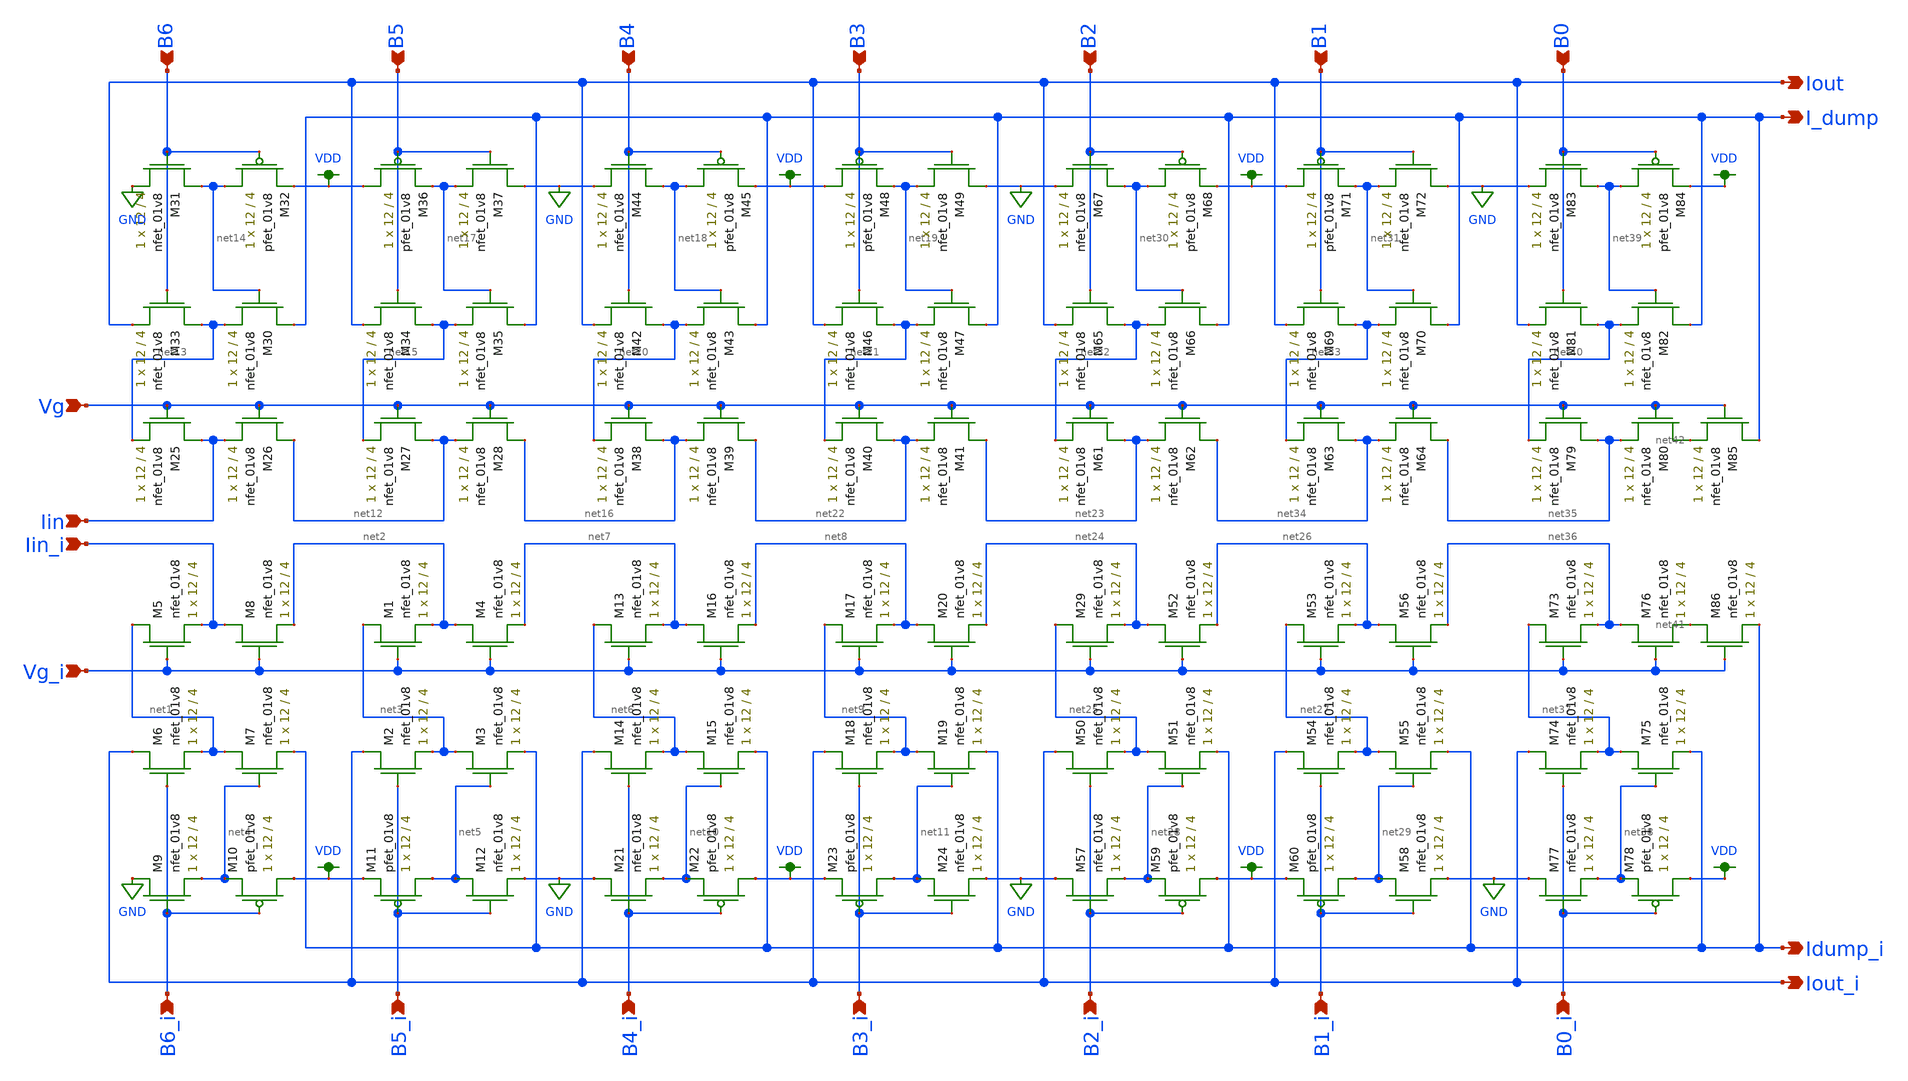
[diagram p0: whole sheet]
** sch_path: modules/ladder_lds.sch
**.subckt ladder_lds Iin_i Vg_i B0_i Idump_i Iout_i B1_i B2_i B3_i Iin Vg B0 B1 B2 B3 I_dump Iout B4
*+ B5 B4_i B5_i B6 B6_i
*.ipin Iin_i
*.ipin Vg_i
*.ipin B0_i
*.opin Idump_i
*.opin Iout_i
*.ipin B1_i
*.ipin B2_i
*.ipin B3_i
*.ipin Iin
*.ipin Vg
*.ipin B0
*.ipin B1
*.ipin B2
*.ipin B3
*.opin I_dump
*.opin Iout
*.ipin B4
*.ipin B5
*.ipin B4_i
*.ipin B5_i
*.ipin B6
*.ipin B6_i
XM5 net1 Vg_i Iin_i GND sky130_fd_pr__nfet_01v8 L=4 W=12 nf=1 ad='int((nf+1)/2) * W/nf * 0.29' as='int((nf+2)/2) * W/nf * 0.29'
+ pd='2*int((nf+1)/2) * (W/nf + 0.29)' ps='2*int((nf+2)/2) * (W/nf + 0.29)' nrd='0.29 / W' nrs='0.29 / W'
+ sa=0 sb=0 sd=0 mult=1 m=1
XM6 Iout_i B6_i net1 GND sky130_fd_pr__nfet_01v8 L=4 W=12 nf=1 ad='int((nf+1)/2) * W/nf * 0.29' as='int((nf+2)/2) * W/nf * 0.29'
+ pd='2*int((nf+1)/2) * (W/nf + 0.29)' ps='2*int((nf+2)/2) * (W/nf + 0.29)' nrd='0.29 / W' nrs='0.29 / W'
+ sa=0 sb=0 sd=0 mult=1 m=1
XM7 net1 net4 Idump_i GND sky130_fd_pr__nfet_01v8 L=4 W=12 nf=1 ad='int((nf+1)/2) * W/nf * 0.29' as='int((nf+2)/2) * W/nf * 0.29'
+ pd='2*int((nf+1)/2) * (W/nf + 0.29)' ps='2*int((nf+2)/2) * (W/nf + 0.29)' nrd='0.29 / W' nrs='0.29 / W'
+ sa=0 sb=0 sd=0 mult=1 m=1
XM8 Iin_i Vg_i net2 GND sky130_fd_pr__nfet_01v8 L=4 W=12 nf=1 ad='int((nf+1)/2) * W/nf * 0.29' as='int((nf+2)/2) * W/nf * 0.29'
+ pd='2*int((nf+1)/2) * (W/nf + 0.29)' ps='2*int((nf+2)/2) * (W/nf + 0.29)' nrd='0.29 / W' nrs='0.29 / W'
+ sa=0 sb=0 sd=0 mult=1 m=1
XM1 net3 Vg_i net2 GND sky130_fd_pr__nfet_01v8 L=4 W=12 nf=1 ad='int((nf+1)/2) * W/nf * 0.29' as='int((nf+2)/2) * W/nf * 0.29'
+ pd='2*int((nf+1)/2) * (W/nf + 0.29)' ps='2*int((nf+2)/2) * (W/nf + 0.29)' nrd='0.29 / W' nrs='0.29 / W'
+ sa=0 sb=0 sd=0 mult=1 m=1
XM2 Iout_i B5_i net3 GND sky130_fd_pr__nfet_01v8 L=4 W=12 nf=1 ad='int((nf+1)/2) * W/nf * 0.29' as='int((nf+2)/2) * W/nf * 0.29'
+ pd='2*int((nf+1)/2) * (W/nf + 0.29)' ps='2*int((nf+2)/2) * (W/nf + 0.29)' nrd='0.29 / W' nrs='0.29 / W'
+ sa=0 sb=0 sd=0 mult=1 m=1
XM3 net3 net5 Idump_i GND sky130_fd_pr__nfet_01v8 L=4 W=12 nf=1 ad='int((nf+1)/2) * W/nf * 0.29' as='int((nf+2)/2) * W/nf * 0.29'
+ pd='2*int((nf+1)/2) * (W/nf + 0.29)' ps='2*int((nf+2)/2) * (W/nf + 0.29)' nrd='0.29 / W' nrs='0.29 / W'
+ sa=0 sb=0 sd=0 mult=1 m=1
XM4 net2 Vg_i net7 GND sky130_fd_pr__nfet_01v8 L=4 W=12 nf=1 ad='int((nf+1)/2) * W/nf * 0.29' as='int((nf+2)/2) * W/nf * 0.29'
+ pd='2*int((nf+1)/2) * (W/nf + 0.29)' ps='2*int((nf+2)/2) * (W/nf + 0.29)' nrd='0.29 / W' nrs='0.29 / W'
+ sa=0 sb=0 sd=0 mult=1 m=1
XM9 GND B6_i net4 GND sky130_fd_pr__nfet_01v8 L=4 W=12 nf=1 ad='int((nf+1)/2) * W/nf * 0.29' as='int((nf+2)/2) * W/nf * 0.29'
+ pd='2*int((nf+1)/2) * (W/nf + 0.29)' ps='2*int((nf+2)/2) * (W/nf + 0.29)' nrd='0.29 / W' nrs='0.29 / W'
+ sa=0 sb=0 sd=0 mult=1 m=1
XM10 VDD B6_i net4 VDD sky130_fd_pr__pfet_01v8 L=4 W=12 nf=1 ad='int((nf+1)/2) * W/nf * 0.29' as='int((nf+2)/2) * W/nf * 0.29'
+ pd='2*int((nf+1)/2) * (W/nf + 0.29)' ps='2*int((nf+2)/2) * (W/nf + 0.29)' nrd='0.29 / W' nrs='0.29 / W'
+ sa=0 sb=0 sd=0 mult=1 m=1
XM12 net5 B5_i GND GND sky130_fd_pr__nfet_01v8 L=4 W=12 nf=1 ad='int((nf+1)/2) * W/nf * 0.29' as='int((nf+2)/2) * W/nf * 0.29'
+ pd='2*int((nf+1)/2) * (W/nf + 0.29)' ps='2*int((nf+2)/2) * (W/nf + 0.29)' nrd='0.29 / W' nrs='0.29 / W'
+ sa=0 sb=0 sd=0 mult=1 m=1
XM13 net6 Vg_i net7 GND sky130_fd_pr__nfet_01v8 L=4 W=12 nf=1 ad='int((nf+1)/2) * W/nf * 0.29' as='int((nf+2)/2) * W/nf * 0.29'
+ pd='2*int((nf+1)/2) * (W/nf + 0.29)' ps='2*int((nf+2)/2) * (W/nf + 0.29)' nrd='0.29 / W' nrs='0.29 / W'
+ sa=0 sb=0 sd=0 mult=1 m=1
XM14 Iout_i B4_i net6 GND sky130_fd_pr__nfet_01v8 L=4 W=12 nf=1 ad='int((nf+1)/2) * W/nf * 0.29' as='int((nf+2)/2) * W/nf * 0.29'
+ pd='2*int((nf+1)/2) * (W/nf + 0.29)' ps='2*int((nf+2)/2) * (W/nf + 0.29)' nrd='0.29 / W' nrs='0.29 / W'
+ sa=0 sb=0 sd=0 mult=1 m=1
XM15 net6 net10 Idump_i GND sky130_fd_pr__nfet_01v8 L=4 W=12 nf=1 ad='int((nf+1)/2) * W/nf * 0.29' as='int((nf+2)/2) * W/nf * 0.29'
+ pd='2*int((nf+1)/2) * (W/nf + 0.29)' ps='2*int((nf+2)/2) * (W/nf + 0.29)' nrd='0.29 / W' nrs='0.29 / W'
+ sa=0 sb=0 sd=0 mult=1 m=1
XM16 net7 Vg_i net8 GND sky130_fd_pr__nfet_01v8 L=4 W=12 nf=1 ad='int((nf+1)/2) * W/nf * 0.29' as='int((nf+2)/2) * W/nf * 0.29'
+ pd='2*int((nf+1)/2) * (W/nf + 0.29)' ps='2*int((nf+2)/2) * (W/nf + 0.29)' nrd='0.29 / W' nrs='0.29 / W'
+ sa=0 sb=0 sd=0 mult=1 m=1
XM17 net9 Vg_i net8 GND sky130_fd_pr__nfet_01v8 L=4 W=12 nf=1 ad='int((nf+1)/2) * W/nf * 0.29' as='int((nf+2)/2) * W/nf * 0.29'
+ pd='2*int((nf+1)/2) * (W/nf + 0.29)' ps='2*int((nf+2)/2) * (W/nf + 0.29)' nrd='0.29 / W' nrs='0.29 / W'
+ sa=0 sb=0 sd=0 mult=1 m=1
XM18 Iout_i B3_i net9 GND sky130_fd_pr__nfet_01v8 L=4 W=12 nf=1 ad='int((nf+1)/2) * W/nf * 0.29' as='int((nf+2)/2) * W/nf * 0.29'
+ pd='2*int((nf+1)/2) * (W/nf + 0.29)' ps='2*int((nf+2)/2) * (W/nf + 0.29)' nrd='0.29 / W' nrs='0.29 / W'
+ sa=0 sb=0 sd=0 mult=1 m=1
XM19 net9 net11 Idump_i GND sky130_fd_pr__nfet_01v8 L=4 W=12 nf=1 ad='int((nf+1)/2) * W/nf * 0.29' as='int((nf+2)/2) * W/nf * 0.29'
+ pd='2*int((nf+1)/2) * (W/nf + 0.29)' ps='2*int((nf+2)/2) * (W/nf + 0.29)' nrd='0.29 / W' nrs='0.29 / W'
+ sa=0 sb=0 sd=0 mult=1 m=1
XM20 net8 Vg_i net24 GND sky130_fd_pr__nfet_01v8 L=4 W=12 nf=1 ad='int((nf+1)/2) * W/nf * 0.29' as='int((nf+2)/2) * W/nf * 0.29'
+ pd='2*int((nf+1)/2) * (W/nf + 0.29)' ps='2*int((nf+2)/2) * (W/nf + 0.29)' nrd='0.29 / W' nrs='0.29 / W'
+ sa=0 sb=0 sd=0 mult=1 m=1
XM21 GND B4_i net10 GND sky130_fd_pr__nfet_01v8 L=4 W=12 nf=1 ad='int((nf+1)/2) * W/nf * 0.29' as='int((nf+2)/2) * W/nf * 0.29'
+ pd='2*int((nf+1)/2) * (W/nf + 0.29)' ps='2*int((nf+2)/2) * (W/nf + 0.29)' nrd='0.29 / W' nrs='0.29 / W'
+ sa=0 sb=0 sd=0 mult=1 m=1
XM24 net11 B3_i GND GND sky130_fd_pr__nfet_01v8 L=4 W=12 nf=1 ad='int((nf+1)/2) * W/nf * 0.29' as='int((nf+2)/2) * W/nf * 0.29'
+ pd='2*int((nf+1)/2) * (W/nf + 0.29)' ps='2*int((nf+2)/2) * (W/nf + 0.29)' nrd='0.29 / W' nrs='0.29 / W'
+ sa=0 sb=0 sd=0 mult=1 m=1
XM11 net5 B5_i VDD VDD sky130_fd_pr__pfet_01v8 L=4 W=12 nf=1 ad='int((nf+1)/2) * W/nf * 0.29' as='int((nf+2)/2) * W/nf * 0.29'
+ pd='2*int((nf+1)/2) * (W/nf + 0.29)' ps='2*int((nf+2)/2) * (W/nf + 0.29)' nrd='0.29 / W' nrs='0.29 / W'
+ sa=0 sb=0 sd=0 mult=1 m=1
XM22 VDD B4_i net10 VDD sky130_fd_pr__pfet_01v8 L=4 W=12 nf=1 ad='int((nf+1)/2) * W/nf * 0.29' as='int((nf+2)/2) * W/nf * 0.29'
+ pd='2*int((nf+1)/2) * (W/nf + 0.29)' ps='2*int((nf+2)/2) * (W/nf + 0.29)' nrd='0.29 / W' nrs='0.29 / W'
+ sa=0 sb=0 sd=0 mult=1 m=1
XM23 net11 B3_i VDD VDD sky130_fd_pr__pfet_01v8 L=4 W=12 nf=1 ad='int((nf+1)/2) * W/nf * 0.29' as='int((nf+2)/2) * W/nf * 0.29'
+ pd='2*int((nf+1)/2) * (W/nf + 0.29)' ps='2*int((nf+2)/2) * (W/nf + 0.29)' nrd='0.29 / W' nrs='0.29 / W'
+ sa=0 sb=0 sd=0 mult=1 m=1
XM25 Iin Vg net13 GND sky130_fd_pr__nfet_01v8 L=4 W=12 nf=1 ad='int((nf+1)/2) * W/nf * 0.29' as='int((nf+2)/2) * W/nf * 0.29'
+ pd='2*int((nf+1)/2) * (W/nf + 0.29)' ps='2*int((nf+2)/2) * (W/nf + 0.29)' nrd='0.29 / W' nrs='0.29 / W'
+ sa=0 sb=0 sd=0 mult=1 m=1
XM26 net12 Vg Iin GND sky130_fd_pr__nfet_01v8 L=4 W=12 nf=1 ad='int((nf+1)/2) * W/nf * 0.29' as='int((nf+2)/2) * W/nf * 0.29'
+ pd='2*int((nf+1)/2) * (W/nf + 0.29)' ps='2*int((nf+2)/2) * (W/nf + 0.29)' nrd='0.29 / W' nrs='0.29 / W'
+ sa=0 sb=0 sd=0 mult=1 m=1
XM27 net12 Vg net15 GND sky130_fd_pr__nfet_01v8 L=4 W=12 nf=1 ad='int((nf+1)/2) * W/nf * 0.29' as='int((nf+2)/2) * W/nf * 0.29'
+ pd='2*int((nf+1)/2) * (W/nf + 0.29)' ps='2*int((nf+2)/2) * (W/nf + 0.29)' nrd='0.29 / W' nrs='0.29 / W'
+ sa=0 sb=0 sd=0 mult=1 m=1
XM28 net16 Vg net12 GND sky130_fd_pr__nfet_01v8 L=4 W=12 nf=1 ad='int((nf+1)/2) * W/nf * 0.29' as='int((nf+2)/2) * W/nf * 0.29'
+ pd='2*int((nf+1)/2) * (W/nf + 0.29)' ps='2*int((nf+2)/2) * (W/nf + 0.29)' nrd='0.29 / W' nrs='0.29 / W'
+ sa=0 sb=0 sd=0 mult=1 m=1
XM30 I_dump net14 net13 GND sky130_fd_pr__nfet_01v8 L=4 W=12 nf=1 ad='int((nf+1)/2) * W/nf * 0.29' as='int((nf+2)/2) * W/nf * 0.29'
+ pd='2*int((nf+1)/2) * (W/nf + 0.29)' ps='2*int((nf+2)/2) * (W/nf + 0.29)' nrd='0.29 / W' nrs='0.29 / W'
+ sa=0 sb=0 sd=0 mult=1 m=1
XM31 net14 B6 GND GND sky130_fd_pr__nfet_01v8 L=4 W=12 nf=1 ad='int((nf+1)/2) * W/nf * 0.29' as='int((nf+2)/2) * W/nf * 0.29'
+ pd='2*int((nf+1)/2) * (W/nf + 0.29)' ps='2*int((nf+2)/2) * (W/nf + 0.29)' nrd='0.29 / W' nrs='0.29 / W'
+ sa=0 sb=0 sd=0 mult=1 m=1
XM32 net14 B6 VDD VDD sky130_fd_pr__pfet_01v8 L=4 W=12 nf=1 ad='int((nf+1)/2) * W/nf * 0.29' as='int((nf+2)/2) * W/nf * 0.29'
+ pd='2*int((nf+1)/2) * (W/nf + 0.29)' ps='2*int((nf+2)/2) * (W/nf + 0.29)' nrd='0.29 / W' nrs='0.29 / W'
+ sa=0 sb=0 sd=0 mult=1 m=1
XM33 net13 B6 Iout GND sky130_fd_pr__nfet_01v8 L=4 W=12 nf=1 ad='int((nf+1)/2) * W/nf * 0.29' as='int((nf+2)/2) * W/nf * 0.29'
+ pd='2*int((nf+1)/2) * (W/nf + 0.29)' ps='2*int((nf+2)/2) * (W/nf + 0.29)' nrd='0.29 / W' nrs='0.29 / W'
+ sa=0 sb=0 sd=0 mult=1 m=1
XM34 net15 B5 Iout GND sky130_fd_pr__nfet_01v8 L=4 W=12 nf=1 ad='int((nf+1)/2) * W/nf * 0.29' as='int((nf+2)/2) * W/nf * 0.29'
+ pd='2*int((nf+1)/2) * (W/nf + 0.29)' ps='2*int((nf+2)/2) * (W/nf + 0.29)' nrd='0.29 / W' nrs='0.29 / W'
+ sa=0 sb=0 sd=0 mult=1 m=1
XM35 I_dump net17 net15 GND sky130_fd_pr__nfet_01v8 L=4 W=12 nf=1 ad='int((nf+1)/2) * W/nf * 0.29' as='int((nf+2)/2) * W/nf * 0.29'
+ pd='2*int((nf+1)/2) * (W/nf + 0.29)' ps='2*int((nf+2)/2) * (W/nf + 0.29)' nrd='0.29 / W' nrs='0.29 / W'
+ sa=0 sb=0 sd=0 mult=1 m=1
XM36 VDD B5 net17 VDD sky130_fd_pr__pfet_01v8 L=4 W=12 nf=1 ad='int((nf+1)/2) * W/nf * 0.29' as='int((nf+2)/2) * W/nf * 0.29'
+ pd='2*int((nf+1)/2) * (W/nf + 0.29)' ps='2*int((nf+2)/2) * (W/nf + 0.29)' nrd='0.29 / W' nrs='0.29 / W'
+ sa=0 sb=0 sd=0 mult=1 m=1
XM37 GND B5 net17 GND sky130_fd_pr__nfet_01v8 L=4 W=12 nf=1 ad='int((nf+1)/2) * W/nf * 0.29' as='int((nf+2)/2) * W/nf * 0.29'
+ pd='2*int((nf+1)/2) * (W/nf + 0.29)' ps='2*int((nf+2)/2) * (W/nf + 0.29)' nrd='0.29 / W' nrs='0.29 / W'
+ sa=0 sb=0 sd=0 mult=1 m=1
XM38 net16 Vg net20 GND sky130_fd_pr__nfet_01v8 L=4 W=12 nf=1 ad='int((nf+1)/2) * W/nf * 0.29' as='int((nf+2)/2) * W/nf * 0.29'
+ pd='2*int((nf+1)/2) * (W/nf + 0.29)' ps='2*int((nf+2)/2) * (W/nf + 0.29)' nrd='0.29 / W' nrs='0.29 / W'
+ sa=0 sb=0 sd=0 mult=1 m=1
XM39 net22 Vg net16 GND sky130_fd_pr__nfet_01v8 L=4 W=12 nf=1 ad='int((nf+1)/2) * W/nf * 0.29' as='int((nf+2)/2) * W/nf * 0.29'
+ pd='2*int((nf+1)/2) * (W/nf + 0.29)' ps='2*int((nf+2)/2) * (W/nf + 0.29)' nrd='0.29 / W' nrs='0.29 / W'
+ sa=0 sb=0 sd=0 mult=1 m=1
XM40 net22 Vg net21 GND sky130_fd_pr__nfet_01v8 L=4 W=12 nf=1 ad='int((nf+1)/2) * W/nf * 0.29' as='int((nf+2)/2) * W/nf * 0.29'
+ pd='2*int((nf+1)/2) * (W/nf + 0.29)' ps='2*int((nf+2)/2) * (W/nf + 0.29)' nrd='0.29 / W' nrs='0.29 / W'
+ sa=0 sb=0 sd=0 mult=1 m=1
XM41 net23 Vg net22 GND sky130_fd_pr__nfet_01v8 L=4 W=12 nf=1 ad='int((nf+1)/2) * W/nf * 0.29' as='int((nf+2)/2) * W/nf * 0.29'
+ pd='2*int((nf+1)/2) * (W/nf + 0.29)' ps='2*int((nf+2)/2) * (W/nf + 0.29)' nrd='0.29 / W' nrs='0.29 / W'
+ sa=0 sb=0 sd=0 mult=1 m=1
XM42 net20 B4 Iout GND sky130_fd_pr__nfet_01v8 L=4 W=12 nf=1 ad='int((nf+1)/2) * W/nf * 0.29' as='int((nf+2)/2) * W/nf * 0.29'
+ pd='2*int((nf+1)/2) * (W/nf + 0.29)' ps='2*int((nf+2)/2) * (W/nf + 0.29)' nrd='0.29 / W' nrs='0.29 / W'
+ sa=0 sb=0 sd=0 mult=1 m=1
XM43 I_dump net18 net20 GND sky130_fd_pr__nfet_01v8 L=4 W=12 nf=1 ad='int((nf+1)/2) * W/nf * 0.29' as='int((nf+2)/2) * W/nf * 0.29'
+ pd='2*int((nf+1)/2) * (W/nf + 0.29)' ps='2*int((nf+2)/2) * (W/nf + 0.29)' nrd='0.29 / W' nrs='0.29 / W'
+ sa=0 sb=0 sd=0 mult=1 m=1
XM44 net18 B4 GND GND sky130_fd_pr__nfet_01v8 L=4 W=12 nf=1 ad='int((nf+1)/2) * W/nf * 0.29' as='int((nf+2)/2) * W/nf * 0.29'
+ pd='2*int((nf+1)/2) * (W/nf + 0.29)' ps='2*int((nf+2)/2) * (W/nf + 0.29)' nrd='0.29 / W' nrs='0.29 / W'
+ sa=0 sb=0 sd=0 mult=1 m=1
XM45 net18 B4 VDD VDD sky130_fd_pr__pfet_01v8 L=4 W=12 nf=1 ad='int((nf+1)/2) * W/nf * 0.29' as='int((nf+2)/2) * W/nf * 0.29'
+ pd='2*int((nf+1)/2) * (W/nf + 0.29)' ps='2*int((nf+2)/2) * (W/nf + 0.29)' nrd='0.29 / W' nrs='0.29 / W'
+ sa=0 sb=0 sd=0 mult=1 m=1
XM46 net21 B3 Iout GND sky130_fd_pr__nfet_01v8 L=4 W=12 nf=1 ad='int((nf+1)/2) * W/nf * 0.29' as='int((nf+2)/2) * W/nf * 0.29'
+ pd='2*int((nf+1)/2) * (W/nf + 0.29)' ps='2*int((nf+2)/2) * (W/nf + 0.29)' nrd='0.29 / W' nrs='0.29 / W'
+ sa=0 sb=0 sd=0 mult=1 m=1
XM47 I_dump net19 net21 GND sky130_fd_pr__nfet_01v8 L=4 W=12 nf=1 ad='int((nf+1)/2) * W/nf * 0.29' as='int((nf+2)/2) * W/nf * 0.29'
+ pd='2*int((nf+1)/2) * (W/nf + 0.29)' ps='2*int((nf+2)/2) * (W/nf + 0.29)' nrd='0.29 / W' nrs='0.29 / W'
+ sa=0 sb=0 sd=0 mult=1 m=1
XM48 VDD B3 net19 VDD sky130_fd_pr__pfet_01v8 L=4 W=12 nf=1 ad='int((nf+1)/2) * W/nf * 0.29' as='int((nf+2)/2) * W/nf * 0.29'
+ pd='2*int((nf+1)/2) * (W/nf + 0.29)' ps='2*int((nf+2)/2) * (W/nf + 0.29)' nrd='0.29 / W' nrs='0.29 / W'
+ sa=0 sb=0 sd=0 mult=1 m=1
XM49 GND B3 net19 GND sky130_fd_pr__nfet_01v8 L=4 W=12 nf=1 ad='int((nf+1)/2) * W/nf * 0.29' as='int((nf+2)/2) * W/nf * 0.29'
+ pd='2*int((nf+1)/2) * (W/nf + 0.29)' ps='2*int((nf+2)/2) * (W/nf + 0.29)' nrd='0.29 / W' nrs='0.29 / W'
+ sa=0 sb=0 sd=0 mult=1 m=1
XM29 net25 Vg_i net24 GND sky130_fd_pr__nfet_01v8 L=4 W=12 nf=1 ad='int((nf+1)/2) * W/nf * 0.29' as='int((nf+2)/2) * W/nf * 0.29'
+ pd='2*int((nf+1)/2) * (W/nf + 0.29)' ps='2*int((nf+2)/2) * (W/nf + 0.29)' nrd='0.29 / W' nrs='0.29 / W'
+ sa=0 sb=0 sd=0 mult=1 m=1
XM50 Iout_i B2_i net25 GND sky130_fd_pr__nfet_01v8 L=4 W=12 nf=1 ad='int((nf+1)/2) * W/nf * 0.29' as='int((nf+2)/2) * W/nf * 0.29'
+ pd='2*int((nf+1)/2) * (W/nf + 0.29)' ps='2*int((nf+2)/2) * (W/nf + 0.29)' nrd='0.29 / W' nrs='0.29 / W'
+ sa=0 sb=0 sd=0 mult=1 m=1
XM51 net25 net28 Idump_i GND sky130_fd_pr__nfet_01v8 L=4 W=12 nf=1 ad='int((nf+1)/2) * W/nf * 0.29' as='int((nf+2)/2) * W/nf * 0.29'
+ pd='2*int((nf+1)/2) * (W/nf + 0.29)' ps='2*int((nf+2)/2) * (W/nf + 0.29)' nrd='0.29 / W' nrs='0.29 / W'
+ sa=0 sb=0 sd=0 mult=1 m=1
XM52 net24 Vg_i net26 GND sky130_fd_pr__nfet_01v8 L=4 W=12 nf=1 ad='int((nf+1)/2) * W/nf * 0.29' as='int((nf+2)/2) * W/nf * 0.29'
+ pd='2*int((nf+1)/2) * (W/nf + 0.29)' ps='2*int((nf+2)/2) * (W/nf + 0.29)' nrd='0.29 / W' nrs='0.29 / W'
+ sa=0 sb=0 sd=0 mult=1 m=1
XM53 net27 Vg_i net26 GND sky130_fd_pr__nfet_01v8 L=4 W=12 nf=1 ad='int((nf+1)/2) * W/nf * 0.29' as='int((nf+2)/2) * W/nf * 0.29'
+ pd='2*int((nf+1)/2) * (W/nf + 0.29)' ps='2*int((nf+2)/2) * (W/nf + 0.29)' nrd='0.29 / W' nrs='0.29 / W'
+ sa=0 sb=0 sd=0 mult=1 m=1
XM54 Iout_i B1_i net27 GND sky130_fd_pr__nfet_01v8 L=4 W=12 nf=1 ad='int((nf+1)/2) * W/nf * 0.29' as='int((nf+2)/2) * W/nf * 0.29'
+ pd='2*int((nf+1)/2) * (W/nf + 0.29)' ps='2*int((nf+2)/2) * (W/nf + 0.29)' nrd='0.29 / W' nrs='0.29 / W'
+ sa=0 sb=0 sd=0 mult=1 m=1
XM55 net27 net29 Idump_i GND sky130_fd_pr__nfet_01v8 L=4 W=12 nf=1 ad='int((nf+1)/2) * W/nf * 0.29' as='int((nf+2)/2) * W/nf * 0.29'
+ pd='2*int((nf+1)/2) * (W/nf + 0.29)' ps='2*int((nf+2)/2) * (W/nf + 0.29)' nrd='0.29 / W' nrs='0.29 / W'
+ sa=0 sb=0 sd=0 mult=1 m=1
XM56 net26 Vg_i net36 GND sky130_fd_pr__nfet_01v8 L=4 W=12 nf=1 ad='int((nf+1)/2) * W/nf * 0.29' as='int((nf+2)/2) * W/nf * 0.29'
+ pd='2*int((nf+1)/2) * (W/nf + 0.29)' ps='2*int((nf+2)/2) * (W/nf + 0.29)' nrd='0.29 / W' nrs='0.29 / W'
+ sa=0 sb=0 sd=0 mult=1 m=1
XM57 GND B2_i net28 GND sky130_fd_pr__nfet_01v8 L=4 W=12 nf=1 ad='int((nf+1)/2) * W/nf * 0.29' as='int((nf+2)/2) * W/nf * 0.29'
+ pd='2*int((nf+1)/2) * (W/nf + 0.29)' ps='2*int((nf+2)/2) * (W/nf + 0.29)' nrd='0.29 / W' nrs='0.29 / W'
+ sa=0 sb=0 sd=0 mult=1 m=1
XM58 net29 B1_i GND GND sky130_fd_pr__nfet_01v8 L=4 W=12 nf=1 ad='int((nf+1)/2) * W/nf * 0.29' as='int((nf+2)/2) * W/nf * 0.29'
+ pd='2*int((nf+1)/2) * (W/nf + 0.29)' ps='2*int((nf+2)/2) * (W/nf + 0.29)' nrd='0.29 / W' nrs='0.29 / W'
+ sa=0 sb=0 sd=0 mult=1 m=1
XM59 VDD B2_i net28 VDD sky130_fd_pr__pfet_01v8 L=4 W=12 nf=1 ad='int((nf+1)/2) * W/nf * 0.29' as='int((nf+2)/2) * W/nf * 0.29'
+ pd='2*int((nf+1)/2) * (W/nf + 0.29)' ps='2*int((nf+2)/2) * (W/nf + 0.29)' nrd='0.29 / W' nrs='0.29 / W'
+ sa=0 sb=0 sd=0 mult=1 m=1
XM60 net29 B1_i VDD VDD sky130_fd_pr__pfet_01v8 L=4 W=12 nf=1 ad='int((nf+1)/2) * W/nf * 0.29' as='int((nf+2)/2) * W/nf * 0.29'
+ pd='2*int((nf+1)/2) * (W/nf + 0.29)' ps='2*int((nf+2)/2) * (W/nf + 0.29)' nrd='0.29 / W' nrs='0.29 / W'
+ sa=0 sb=0 sd=0 mult=1 m=1
XM61 net23 Vg net32 GND sky130_fd_pr__nfet_01v8 L=4 W=12 nf=1 ad='int((nf+1)/2) * W/nf * 0.29' as='int((nf+2)/2) * W/nf * 0.29'
+ pd='2*int((nf+1)/2) * (W/nf + 0.29)' ps='2*int((nf+2)/2) * (W/nf + 0.29)' nrd='0.29 / W' nrs='0.29 / W'
+ sa=0 sb=0 sd=0 mult=1 m=1
XM62 net34 Vg net23 GND sky130_fd_pr__nfet_01v8 L=4 W=12 nf=1 ad='int((nf+1)/2) * W/nf * 0.29' as='int((nf+2)/2) * W/nf * 0.29'
+ pd='2*int((nf+1)/2) * (W/nf + 0.29)' ps='2*int((nf+2)/2) * (W/nf + 0.29)' nrd='0.29 / W' nrs='0.29 / W'
+ sa=0 sb=0 sd=0 mult=1 m=1
XM63 net34 Vg net33 GND sky130_fd_pr__nfet_01v8 L=4 W=12 nf=1 ad='int((nf+1)/2) * W/nf * 0.29' as='int((nf+2)/2) * W/nf * 0.29'
+ pd='2*int((nf+1)/2) * (W/nf + 0.29)' ps='2*int((nf+2)/2) * (W/nf + 0.29)' nrd='0.29 / W' nrs='0.29 / W'
+ sa=0 sb=0 sd=0 mult=1 m=1
XM64 net35 Vg net34 GND sky130_fd_pr__nfet_01v8 L=4 W=12 nf=1 ad='int((nf+1)/2) * W/nf * 0.29' as='int((nf+2)/2) * W/nf * 0.29'
+ pd='2*int((nf+1)/2) * (W/nf + 0.29)' ps='2*int((nf+2)/2) * (W/nf + 0.29)' nrd='0.29 / W' nrs='0.29 / W'
+ sa=0 sb=0 sd=0 mult=1 m=1
XM65 net32 B2 Iout GND sky130_fd_pr__nfet_01v8 L=4 W=12 nf=1 ad='int((nf+1)/2) * W/nf * 0.29' as='int((nf+2)/2) * W/nf * 0.29'
+ pd='2*int((nf+1)/2) * (W/nf + 0.29)' ps='2*int((nf+2)/2) * (W/nf + 0.29)' nrd='0.29 / W' nrs='0.29 / W'
+ sa=0 sb=0 sd=0 mult=1 m=1
XM66 I_dump net30 net32 GND sky130_fd_pr__nfet_01v8 L=4 W=12 nf=1 ad='int((nf+1)/2) * W/nf * 0.29' as='int((nf+2)/2) * W/nf * 0.29'
+ pd='2*int((nf+1)/2) * (W/nf + 0.29)' ps='2*int((nf+2)/2) * (W/nf + 0.29)' nrd='0.29 / W' nrs='0.29 / W'
+ sa=0 sb=0 sd=0 mult=1 m=1
XM67 net30 B2 GND GND sky130_fd_pr__nfet_01v8 L=4 W=12 nf=1 ad='int((nf+1)/2) * W/nf * 0.29' as='int((nf+2)/2) * W/nf * 0.29'
+ pd='2*int((nf+1)/2) * (W/nf + 0.29)' ps='2*int((nf+2)/2) * (W/nf + 0.29)' nrd='0.29 / W' nrs='0.29 / W'
+ sa=0 sb=0 sd=0 mult=1 m=1
XM68 net30 B2 VDD VDD sky130_fd_pr__pfet_01v8 L=4 W=12 nf=1 ad='int((nf+1)/2) * W/nf * 0.29' as='int((nf+2)/2) * W/nf * 0.29'
+ pd='2*int((nf+1)/2) * (W/nf + 0.29)' ps='2*int((nf+2)/2) * (W/nf + 0.29)' nrd='0.29 / W' nrs='0.29 / W'
+ sa=0 sb=0 sd=0 mult=1 m=1
XM69 net33 B1 Iout GND sky130_fd_pr__nfet_01v8 L=4 W=12 nf=1 ad='int((nf+1)/2) * W/nf * 0.29' as='int((nf+2)/2) * W/nf * 0.29'
+ pd='2*int((nf+1)/2) * (W/nf + 0.29)' ps='2*int((nf+2)/2) * (W/nf + 0.29)' nrd='0.29 / W' nrs='0.29 / W'
+ sa=0 sb=0 sd=0 mult=1 m=1
XM70 I_dump net31 net33 GND sky130_fd_pr__nfet_01v8 L=4 W=12 nf=1 ad='int((nf+1)/2) * W/nf * 0.29' as='int((nf+2)/2) * W/nf * 0.29'
+ pd='2*int((nf+1)/2) * (W/nf + 0.29)' ps='2*int((nf+2)/2) * (W/nf + 0.29)' nrd='0.29 / W' nrs='0.29 / W'
+ sa=0 sb=0 sd=0 mult=1 m=1
XM71 VDD B1 net31 VDD sky130_fd_pr__pfet_01v8 L=4 W=12 nf=1 ad='int((nf+1)/2) * W/nf * 0.29' as='int((nf+2)/2) * W/nf * 0.29'
+ pd='2*int((nf+1)/2) * (W/nf + 0.29)' ps='2*int((nf+2)/2) * (W/nf + 0.29)' nrd='0.29 / W' nrs='0.29 / W'
+ sa=0 sb=0 sd=0 mult=1 m=1
XM72 GND B1 net31 GND sky130_fd_pr__nfet_01v8 L=4 W=12 nf=1 ad='int((nf+1)/2) * W/nf * 0.29' as='int((nf+2)/2) * W/nf * 0.29'
+ pd='2*int((nf+1)/2) * (W/nf + 0.29)' ps='2*int((nf+2)/2) * (W/nf + 0.29)' nrd='0.29 / W' nrs='0.29 / W'
+ sa=0 sb=0 sd=0 mult=1 m=1
XM73 net37 Vg_i net36 GND sky130_fd_pr__nfet_01v8 L=4 W=12 nf=1 ad='int((nf+1)/2) * W/nf * 0.29' as='int((nf+2)/2) * W/nf * 0.29'
+ pd='2*int((nf+1)/2) * (W/nf + 0.29)' ps='2*int((nf+2)/2) * (W/nf + 0.29)' nrd='0.29 / W' nrs='0.29 / W'
+ sa=0 sb=0 sd=0 mult=1 m=1
XM74 Iout_i B0_i net37 GND sky130_fd_pr__nfet_01v8 L=4 W=12 nf=1 ad='int((nf+1)/2) * W/nf * 0.29' as='int((nf+2)/2) * W/nf * 0.29'
+ pd='2*int((nf+1)/2) * (W/nf + 0.29)' ps='2*int((nf+2)/2) * (W/nf + 0.29)' nrd='0.29 / W' nrs='0.29 / W'
+ sa=0 sb=0 sd=0 mult=1 m=1
XM75 net37 net38 Idump_i GND sky130_fd_pr__nfet_01v8 L=4 W=12 nf=1 ad='int((nf+1)/2) * W/nf * 0.29' as='int((nf+2)/2) * W/nf * 0.29'
+ pd='2*int((nf+1)/2) * (W/nf + 0.29)' ps='2*int((nf+2)/2) * (W/nf + 0.29)' nrd='0.29 / W' nrs='0.29 / W'
+ sa=0 sb=0 sd=0 mult=1 m=1
XM76 net36 Vg_i net41 GND sky130_fd_pr__nfet_01v8 L=4 W=12 nf=1 ad='int((nf+1)/2) * W/nf * 0.29' as='int((nf+2)/2) * W/nf * 0.29'
+ pd='2*int((nf+1)/2) * (W/nf + 0.29)' ps='2*int((nf+2)/2) * (W/nf + 0.29)' nrd='0.29 / W' nrs='0.29 / W'
+ sa=0 sb=0 sd=0 mult=1 m=1
XM77 GND B0_i net38 GND sky130_fd_pr__nfet_01v8 L=4 W=12 nf=1 ad='int((nf+1)/2) * W/nf * 0.29' as='int((nf+2)/2) * W/nf * 0.29'
+ pd='2*int((nf+1)/2) * (W/nf + 0.29)' ps='2*int((nf+2)/2) * (W/nf + 0.29)' nrd='0.29 / W' nrs='0.29 / W'
+ sa=0 sb=0 sd=0 mult=1 m=1
XM78 VDD B0_i net38 VDD sky130_fd_pr__pfet_01v8 L=4 W=12 nf=1 ad='int((nf+1)/2) * W/nf * 0.29' as='int((nf+2)/2) * W/nf * 0.29'
+ pd='2*int((nf+1)/2) * (W/nf + 0.29)' ps='2*int((nf+2)/2) * (W/nf + 0.29)' nrd='0.29 / W' nrs='0.29 / W'
+ sa=0 sb=0 sd=0 mult=1 m=1
XM79 net35 Vg net40 GND sky130_fd_pr__nfet_01v8 L=4 W=12 nf=1 ad='int((nf+1)/2) * W/nf * 0.29' as='int((nf+2)/2) * W/nf * 0.29'
+ pd='2*int((nf+1)/2) * (W/nf + 0.29)' ps='2*int((nf+2)/2) * (W/nf + 0.29)' nrd='0.29 / W' nrs='0.29 / W'
+ sa=0 sb=0 sd=0 mult=1 m=1
XM80 net42 Vg net35 GND sky130_fd_pr__nfet_01v8 L=4 W=12 nf=1 ad='int((nf+1)/2) * W/nf * 0.29' as='int((nf+2)/2) * W/nf * 0.29'
+ pd='2*int((nf+1)/2) * (W/nf + 0.29)' ps='2*int((nf+2)/2) * (W/nf + 0.29)' nrd='0.29 / W' nrs='0.29 / W'
+ sa=0 sb=0 sd=0 mult=1 m=1
XM81 net40 B0 Iout GND sky130_fd_pr__nfet_01v8 L=4 W=12 nf=1 ad='int((nf+1)/2) * W/nf * 0.29' as='int((nf+2)/2) * W/nf * 0.29'
+ pd='2*int((nf+1)/2) * (W/nf + 0.29)' ps='2*int((nf+2)/2) * (W/nf + 0.29)' nrd='0.29 / W' nrs='0.29 / W'
+ sa=0 sb=0 sd=0 mult=1 m=1
XM82 I_dump net39 net40 GND sky130_fd_pr__nfet_01v8 L=4 W=12 nf=1 ad='int((nf+1)/2) * W/nf * 0.29' as='int((nf+2)/2) * W/nf * 0.29'
+ pd='2*int((nf+1)/2) * (W/nf + 0.29)' ps='2*int((nf+2)/2) * (W/nf + 0.29)' nrd='0.29 / W' nrs='0.29 / W'
+ sa=0 sb=0 sd=0 mult=1 m=1
XM83 net39 B0 GND GND sky130_fd_pr__nfet_01v8 L=4 W=12 nf=1 ad='int((nf+1)/2) * W/nf * 0.29' as='int((nf+2)/2) * W/nf * 0.29'
+ pd='2*int((nf+1)/2) * (W/nf + 0.29)' ps='2*int((nf+2)/2) * (W/nf + 0.29)' nrd='0.29 / W' nrs='0.29 / W'
+ sa=0 sb=0 sd=0 mult=1 m=1
XM84 net39 B0 VDD VDD sky130_fd_pr__pfet_01v8 L=4 W=12 nf=1 ad='int((nf+1)/2) * W/nf * 0.29' as='int((nf+2)/2) * W/nf * 0.29'
+ pd='2*int((nf+1)/2) * (W/nf + 0.29)' ps='2*int((nf+2)/2) * (W/nf + 0.29)' nrd='0.29 / W' nrs='0.29 / W'
+ sa=0 sb=0 sd=0 mult=1 m=1
XM85 I_dump Vg net42 GND sky130_fd_pr__nfet_01v8 L=4 W=12 nf=1 ad='int((nf+1)/2) * W/nf * 0.29' as='int((nf+2)/2) * W/nf * 0.29'
+ pd='2*int((nf+1)/2) * (W/nf + 0.29)' ps='2*int((nf+2)/2) * (W/nf + 0.29)' nrd='0.29 / W' nrs='0.29 / W'
+ sa=0 sb=0 sd=0 mult=1 m=1
XM86 net41 Vg_i Idump_i GND sky130_fd_pr__nfet_01v8 L=4 W=12 nf=1 ad='int((nf+1)/2) * W/nf * 0.29' as='int((nf+2)/2) * W/nf * 0.29'
+ pd='2*int((nf+1)/2) * (W/nf + 0.29)' ps='2*int((nf+2)/2) * (W/nf + 0.29)' nrd='0.29 / W' nrs='0.29 / W'
+ sa=0 sb=0 sd=0 mult=1 m=1
**.ends
.GLOBAL GND
.GLOBAL VDD
.end
